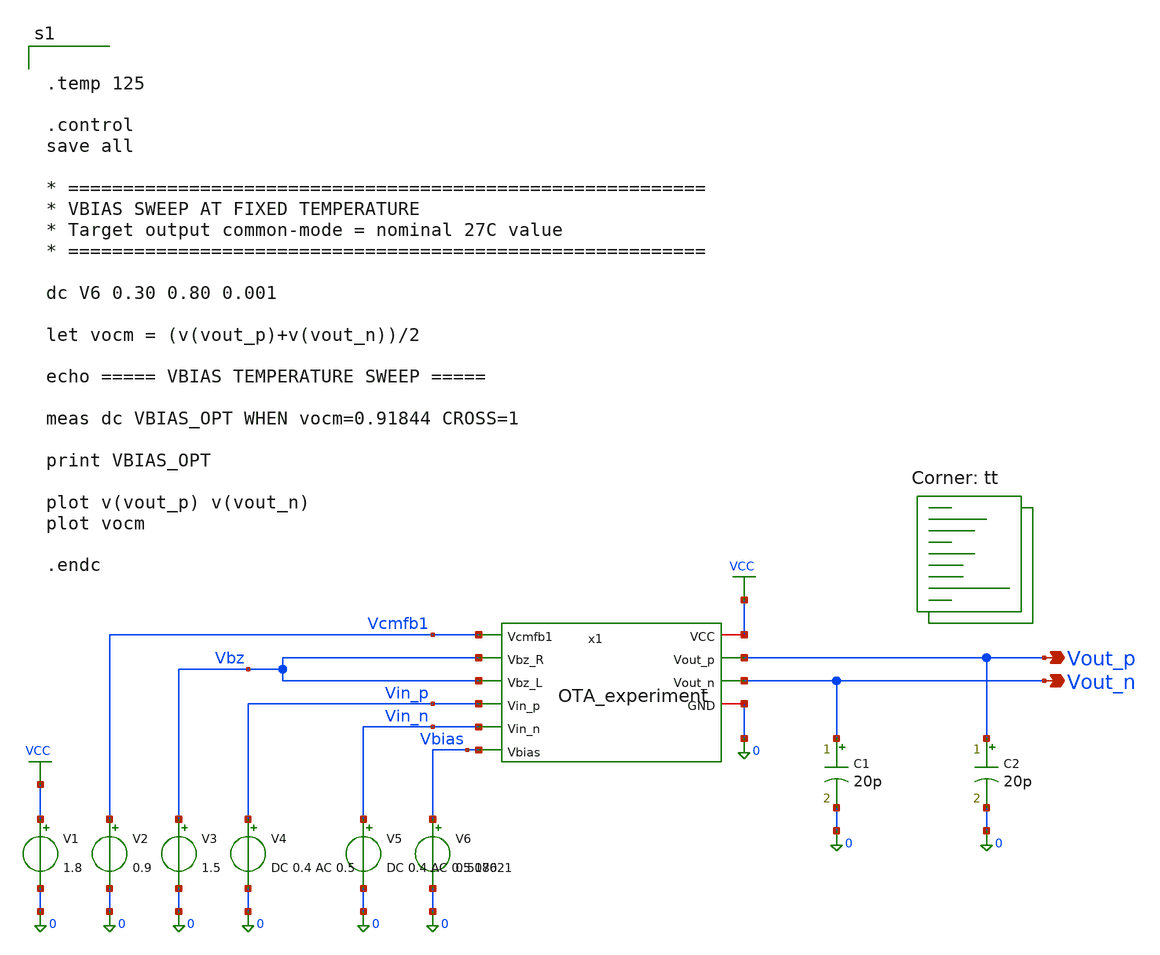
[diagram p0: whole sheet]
** sch_path: blocks/01_OTA/sim/tb_OTA_BIAS_TEMP_experiment.sch
**.subckt tb_OTA_BIAS_TEMP_experiment Vout_p Vout_n
*.opin Vout_p
*.opin Vout_n
V1 VCC 0 1.8
V2 Vcmfb1 0 0.9
V3 Vbz 0 1.5
V4 Vin_p 0 DC 0.4 AC 0.5
V5 Vin_n 0 DC 0.4 AC 0.5 180
V6 Vbias 0 0.507621
C1 Vout_n 0 20p m=1
C2 Vout_p 0 20p m=1
x1 VCC Vcmfb1 Vbz Vbz Vin_p Vin_n Vout_p Vout_n Vbias 0 OTA_experiment
**** begin user architecture code


.temp 125

.control
save all

* ==========================================================
* VBIAS SWEEP AT FIXED TEMPERATURE
* Target output common-mode = nominal 27C value
* ==========================================================

dc V6 0.30 0.80 0.001

let vocm = (v(vout_p)+v(vout_n))/2

echo ===== VBIAS TEMPERATURE SWEEP =====

meas dc VBIAS_OPT WHEN vocm=0.91844 CROSS=1

print VBIAS_OPT

plot v(vout_p) v(vout_n)
plot vocm

.endc


.lib $::SKYWATER_MODELS/sky130.lib.spice tt
**** end user architecture code
**.ends

* expanding   symbol:  blocks/01_OTA/xschem/OTA_experiment.sym # of pins=10
** sym_path: blocks/01_OTA/xschem/OTA_experiment.sym
** sch_path: blocks/01_OTA/xschem/OTA_experiment.sch
.subckt OTA_experiment VCC Vcmfb1 Vbz_R Vbz_L Vin_p Vin_n Vout_p Vout_n Vbias GND
*.ipin Vin_p
*.ipin Vin_n
*.ipin Vbias
*.ipin Vbz_R
*.ipin Vbz_L
*.ipin Vcmfb1
*.opin Vout_p
*.opin Vout_n
*.iopin VCC
*.iopin GND
XM1 net5 Vin_p net3 net5 sky130_fd_pr__pfet_01v8 L=1.2 W=120 nf=1 ad='int((1 + 1)/2) * 120 / 1 * 0.29'
+ as='int((1 + 2)/2) * 120 / 1 * 0.29' pd='2*int((1 + 1)/2) * (120 / 1 + 0.29)' ps='2*int((1 + 2)/2) * (120 / 1 + 0.29)'
+ nrd='0.29 / 120 ' nrs='0.29 / 120 ' sa=0 sb=0 sd=0 mult=1 m=1
XM2 net5 Vin_n net4 net5 sky130_fd_pr__pfet_01v8 L=1.2 W=120 nf=1 ad='int((1 + 1)/2) * 120 / 1 * 0.29'
+ as='int((1 + 2)/2) * 120 / 1 * 0.29' pd='2*int((1 + 1)/2) * (120 / 1 + 0.29)' ps='2*int((1 + 2)/2) * (120 / 1 + 0.29)'
+ nrd='0.29 / 120 ' nrs='0.29 / 120 ' sa=0 sb=0 sd=0 mult=1 m=1
XM3 net3 Vbias GND GND sky130_fd_pr__nfet_01v8 L=2 W=8 nf=1 ad='int((1 + 1)/2) * 8 / 1 * 0.29' as='int((1 + 2)/2) * 8 / 1 * 0.29'
+ pd='2*int((1 + 1)/2) * (8 / 1 + 0.29)' ps='2*int((1 + 2)/2) * (8 / 1 + 0.29)' nrd='0.29 / 8 ' nrs='0.29 / 8 '
+ sa=0 sb=0 sd=0 mult=1 m=1
XM4 net4 Vbias GND GND sky130_fd_pr__nfet_01v8 L=2 W=8 nf=1 ad='int((1 + 1)/2) * 8 / 1 * 0.29' as='int((1 + 2)/2) * 8 / 1 * 0.29'
+ pd='2*int((1 + 1)/2) * (8 / 1 + 0.29)' ps='2*int((1 + 2)/2) * (8 / 1 + 0.29)' nrd='0.29 / 8 ' nrs='0.29 / 8 '
+ sa=0 sb=0 sd=0 mult=1 m=1
XM5 net1 net4 GND GND sky130_fd_pr__nfet_01v8 L=2 W=20 nf=1 ad='int((1 + 1)/2) * 20 / 1 * 0.29' as='int((1 + 2)/2) * 20 / 1 * 0.29'
+ pd='2*int((1 + 1)/2) * (20 / 1 + 0.29)' ps='2*int((1 + 2)/2) * (20 / 1 + 0.29)' nrd='0.29 / 20 ' nrs='0.29 / 20 '
+ sa=0 sb=0 sd=0 mult=1 m=1
XM6 net2 net3 GND GND sky130_fd_pr__nfet_01v8 L=2 W=20 nf=1 ad='int((1 + 1)/2) * 20 / 1 * 0.29' as='int((1 + 2)/2) * 20 / 1 * 0.29'
+ pd='2*int((1 + 1)/2) * (20 / 1 + 0.29)' ps='2*int((1 + 2)/2) * (20 / 1 + 0.29)' nrd='0.29 / 20 ' nrs='0.29 / 20 '
+ sa=0 sb=0 sd=0 mult=1 m=1
XM7 VCC net1 net1 VCC sky130_fd_pr__pfet_01v8 L=2 W=30 nf=1 ad='int((1 + 1)/2) * 30 / 1 * 0.29' as='int((1 + 2)/2) * 30 / 1 * 0.29'
+ pd='2*int((1 + 1)/2) * (30 / 1 + 0.29)' ps='2*int((1 + 2)/2) * (30 / 1 + 0.29)' nrd='0.29 / 30 ' nrs='0.29 / 30 '
+ sa=0 sb=0 sd=0 mult=1 m=1
XM8 VCC net2 net2 VCC sky130_fd_pr__pfet_01v8 L=2 W=30 nf=1 ad='int((1 + 1)/2) * 30 / 1 * 0.29' as='int((1 + 2)/2) * 30 / 1 * 0.29'
+ pd='2*int((1 + 1)/2) * (30 / 1 + 0.29)' ps='2*int((1 + 2)/2) * (30 / 1 + 0.29)' nrd='0.29 / 30 ' nrs='0.29 / 30 '
+ sa=0 sb=0 sd=0 mult=1 m=1
XM9 VCC net1 Vout_p VCC sky130_fd_pr__pfet_01v8 L=1 W=300 nf=1 ad='int((1 + 1)/2) * 300 / 1 * 0.29' as='int((1 + 2)/2) * 300 / 1 * 0.29'
+ pd='2*int((1 + 1)/2) * (300 / 1 + 0.29)' ps='2*int((1 + 2)/2) * (300 / 1 + 0.29)' nrd='0.29 / 300 ' nrs='0.29 / 300 '
+ sa=0 sb=0 sd=0 mult=1 m=1
XM10 VCC net2 Vout_n VCC sky130_fd_pr__pfet_01v8 L=1 W=300 nf=1 ad='int((1 + 1)/2) * 300 / 1 * 0.29'
+ as='int((1 + 2)/2) * 300 / 1 * 0.29' pd='2*int((1 + 1)/2) * (300 / 1 + 0.29)' ps='2*int((1 + 2)/2) * (300 / 1 + 0.29)'
+ nrd='0.29 / 300 ' nrs='0.29 / 300 ' sa=0 sb=0 sd=0 mult=1 m=1
XM11 Vout_p net4 GND GND sky130_fd_pr__nfet_01v8 L=1 W=200 nf=1 ad='int((1 + 1)/2) * 200 / 1 * 0.29'
+ as='int((1 + 2)/2) * 200 / 1 * 0.29' pd='2*int((1 + 1)/2) * (200 / 1 + 0.29)' ps='2*int((1 + 2)/2) * (200 / 1 + 0.29)'
+ nrd='0.29 / 200 ' nrs='0.29 / 200 ' sa=0 sb=0 sd=0 mult=1 m=1
XM12 Vout_n net3 GND GND sky130_fd_pr__nfet_01v8 L=1 W=200 nf=1 ad='int((1 + 1)/2) * 200 / 1 * 0.29'
+ as='int((1 + 2)/2) * 200 / 1 * 0.29' pd='2*int((1 + 1)/2) * (200 / 1 + 0.29)' ps='2*int((1 + 2)/2) * (200 / 1 + 0.29)'
+ nrd='0.29 / 200 ' nrs='0.29 / 200 ' sa=0 sb=0 sd=0 mult=1 m=1
XM13 VCC Vcmfb1 net5 VCC sky130_fd_pr__pfet_01v8 L=1.2 W=60 nf=1 ad='int((1 + 1)/2) * 60 / 1 * 0.29'
+ as='int((1 + 2)/2) * 60 / 1 * 0.29' pd='2*int((1 + 1)/2) * (60 / 1 + 0.29)' ps='2*int((1 + 2)/2) * (60 / 1 + 0.29)'
+ nrd='0.29 / 60 ' nrs='0.29 / 60 ' sa=0 sb=0 sd=0 mult=1 m=1
XC1 Vout_p net4 sky130_fd_pr__cap_mim_m3_1 W=1 L=1 MF=80 m=80
XC2 net3 Vout_n sky130_fd_pr__cap_mim_m3_1 W=1 L=1 MF=80 m=80
.ends

.GLOBAL VCC
.end
